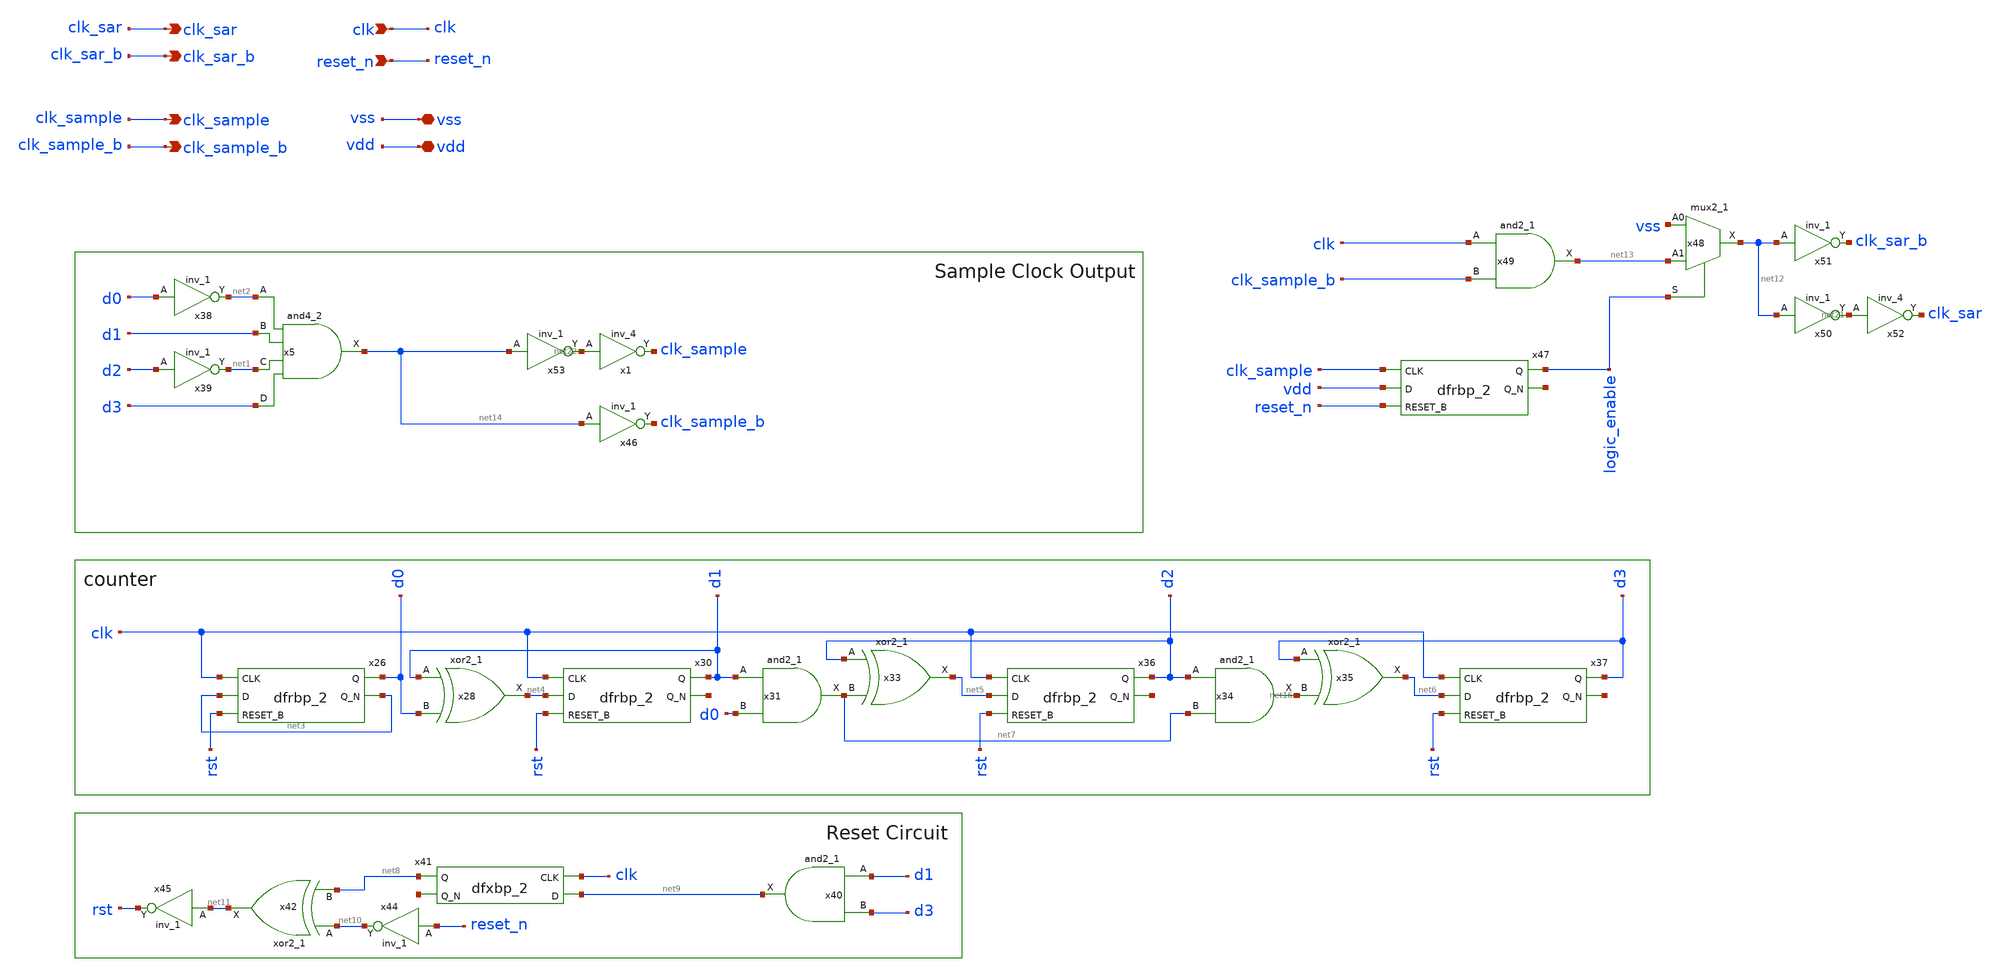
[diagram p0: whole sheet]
** sch_path: xschem/clockgen/clockgen.sch
**.subckt clockgen clk_sar clk_sample clk vss vdd clk_sar_b clk_sample_b reset_n
*.opin clk_sar
*.opin clk_sample
*.ipin clk
*.iopin vss
*.iopin vdd
*.opin clk_sar_b
*.opin clk_sample_b
*.ipin reset_n
x5 net2 d1 net1 d3 vss vss vdd vdd net14 sky130_fd_sc_hd__and4_2
x26 clk net3 rst vss vss vdd vdd d0 net3 sky130_fd_sc_hd__dfrbp_2
x28 d1 d0 vss vss vdd vdd net4 sky130_fd_sc_hd__xor2_1
x30 clk net4 rst vss vss vdd vdd d1 net15 sky130_fd_sc_hd__dfrbp_2
x31 d1 d0 vss vss vdd vdd net7 sky130_fd_sc_hd__and2_1
x33 d2 net7 vss vss vdd vdd net5 sky130_fd_sc_hd__xor2_1
x34 d2 net7 vss vss vdd vdd net16 sky130_fd_sc_hd__and2_1
x35 d3 net16 vss vss vdd vdd net6 sky130_fd_sc_hd__xor2_1
x36 clk net5 rst vss vss vdd vdd d2 net17 sky130_fd_sc_hd__dfrbp_2
x37 clk net6 rst vss vss vdd vdd d3 net18 sky130_fd_sc_hd__dfrbp_2
x38 d0 vss vss vdd vdd net2 sky130_fd_sc_hd__inv_1
x39 d2 vss vss vdd vdd net1 sky130_fd_sc_hd__inv_1
x40 d1 d3 vss vss vdd vdd net9 sky130_fd_sc_hd__and2_1
x41 clk net9 vss vss vdd vdd net8 net19 sky130_fd_sc_hd__dfxbp_2
x42 net10 net8 vss vss vdd vdd net11 sky130_fd_sc_hd__xor2_1
x44 reset_n vss vss vdd vdd net10 sky130_fd_sc_hd__inv_1
x45 net11 vss vss vdd vdd rst sky130_fd_sc_hd__inv_1
x46 net14 vss vss vdd vdd clk_sample_b sky130_fd_sc_hd__inv_1
x47 clk_sample vdd reset_n vss vss vdd vdd logic_enable net20 sky130_fd_sc_hd__dfrbp_2
x48 vss net13 logic_enable vss vss vdd vdd net12 sky130_fd_sc_hd__mux2_1
x49 clk clk_sample_b vss vss vdd vdd net13 sky130_fd_sc_hd__and2_1
x50 net12 vss vss vdd vdd net21 sky130_fd_sc_hd__inv_1
x51 net12 vss vss vdd vdd clk_sar_b sky130_fd_sc_hd__inv_1
x52 net21 vss vss vdd vdd clk_sar sky130_fd_sc_hd__inv_4
x53 net14 vss vss vdd vdd net22 sky130_fd_sc_hd__inv_1
x1 net22 vss vss vdd vdd clk_sample sky130_fd_sc_hd__inv_4
**.ends
.end
